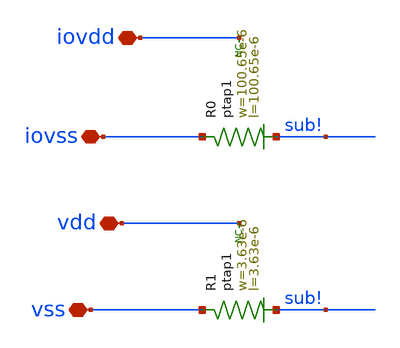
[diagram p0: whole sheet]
** sch_path: ihp-sg13g2/libs.ref/sg13g2_io/sch/xschem/sg13g2_Corner.sch
**.subckt sg13g2_Corner iovdd iovss vdd vss
*.iopin iovdd
*.iopin iovss
*.iopin vdd
*.iopin vss
* noconn iovdd
* noconn vdd
XR0 iovss sub! ptap1 R=93.04m w=100.65e-6 l=100.65e-6
XR1 vss sub! ptap1 R=35.38 w=3.63e-6 l=3.63e-6
**.ends
.end
